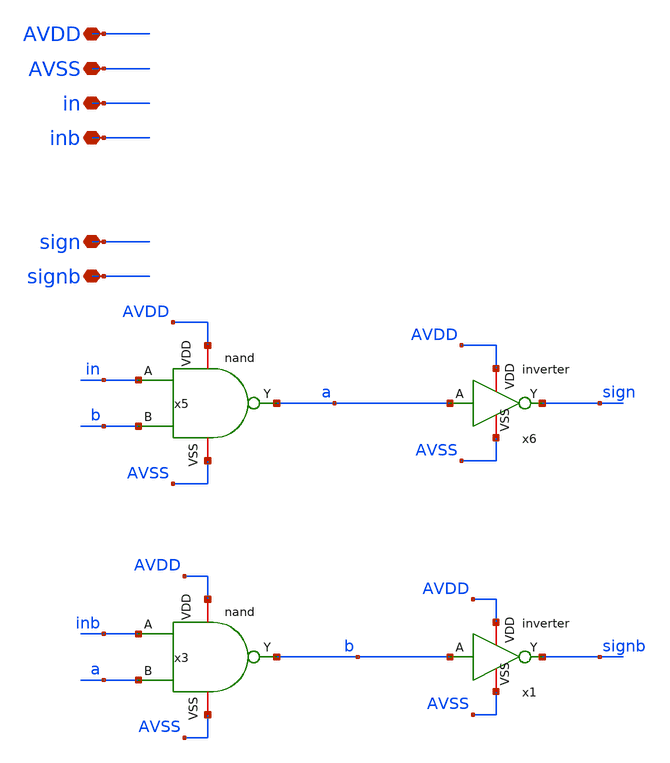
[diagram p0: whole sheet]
** sch_path: current_generator/analog/DAC/schematics/non_overlap.sch
**.subckt non_overlap AVDD AVSS in inb sign signb
*.iopin AVDD
*.iopin AVSS
*.iopin in
*.iopin inb
*.iopin sign
*.iopin signb
x5 AVDD AVSS in b a nand
x6 a sign AVDD AVSS inverter
x3 AVDD AVSS inb a b nand
x1 b signb AVDD AVSS inverter
**.ends

* expanding   symbol:  nand.sym # of pins=5
** sym_path: current_generator/analog/DAC/schematics/nand.sym
** sch_path: current_generator/analog/DAC/schematics/nand.sch
.subckt nand VDD VSS A B Y
*.opin Y
*.ipin A
*.iopin VDD
*.iopin VSS
*.ipin B
XMN0 net1 B VSS VSS sg13_lv_nmos w=1.44u l=130.00n ng=2 m=1 mm_ok=1
XMP0 Y B VDD VDD sg13_lv_pmos w=2.24u l=130.00n ng=2 m=1 mm_ok=1
XMN1 Y A net1 VSS sg13_lv_nmos w=1.44u l=130.00n ng=2 m=1 mm_ok=1
XMP1 Y A VDD VDD sg13_lv_pmos w=2.24u l=130.00n ng=2 m=1 mm_ok=1
.ends


* expanding   symbol:  inverter.sym # of pins=4
** sym_path: current_generator/analog/DAC/schematics/inverter.sym
** sch_path: current_generator/analog/DAC/schematics/inverter.sch
.subckt inverter A Y VDD VSS
*.opin Y
*.ipin A
*.iopin VDD
*.iopin VSS
MMN0 Y A VSS VSS sg13_lv_nmos w=740.00n l=130.00n ng=1 m=1 mm_ok=1
MMP0 Y A VDD VDD sg13_lv_pmos w=1.12u l=130.00n ng=1 m=1 mm_ok=1
.ends

.end
